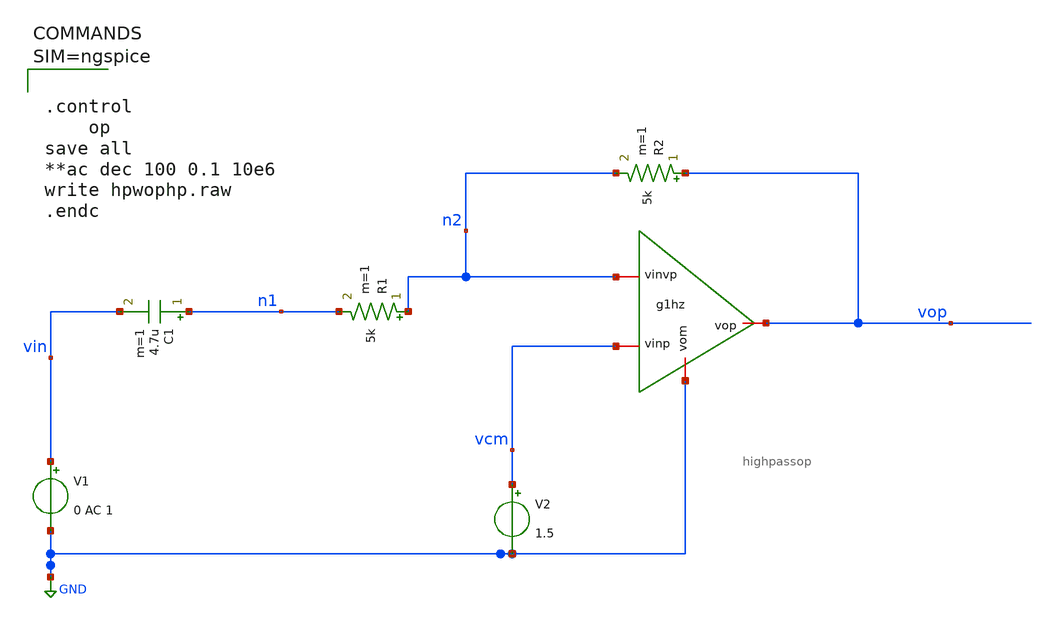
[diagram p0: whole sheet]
** sch_path: hpwophp.sch
**.subckt hpwophp
V1 vin GND 0 AC 1
R1 n2 n1 5k m=1
C1 n1 vin 4.7u m=1
V2 vcm GND 1.5
R2 vop n2 5k m=1
x1 vcm GND vop n2 highpassop
**** begin user architecture code



.control
	op
save all
**ac dec 100 0.1 10e6
write hpwophp.raw
.endc



**** end user architecture code
**.ends

* expanding   symbol:  highpassop.sym # of pins=4
** sym_path: highpassop.sym
** sch_path: highpassop.sch
.subckt highpassop vinp vom vop vinvp
*.iopin vinp
*.iopin vinvp
*.iopin vop
*.iopin vom
E1 net1 GND vinp vinvp 1000
E2 vop vom net2 GND 1
R1 net2 net1 15.9k m=1
C1 net2 GND 10n m=1
.ends

.GLOBAL GND
.end
